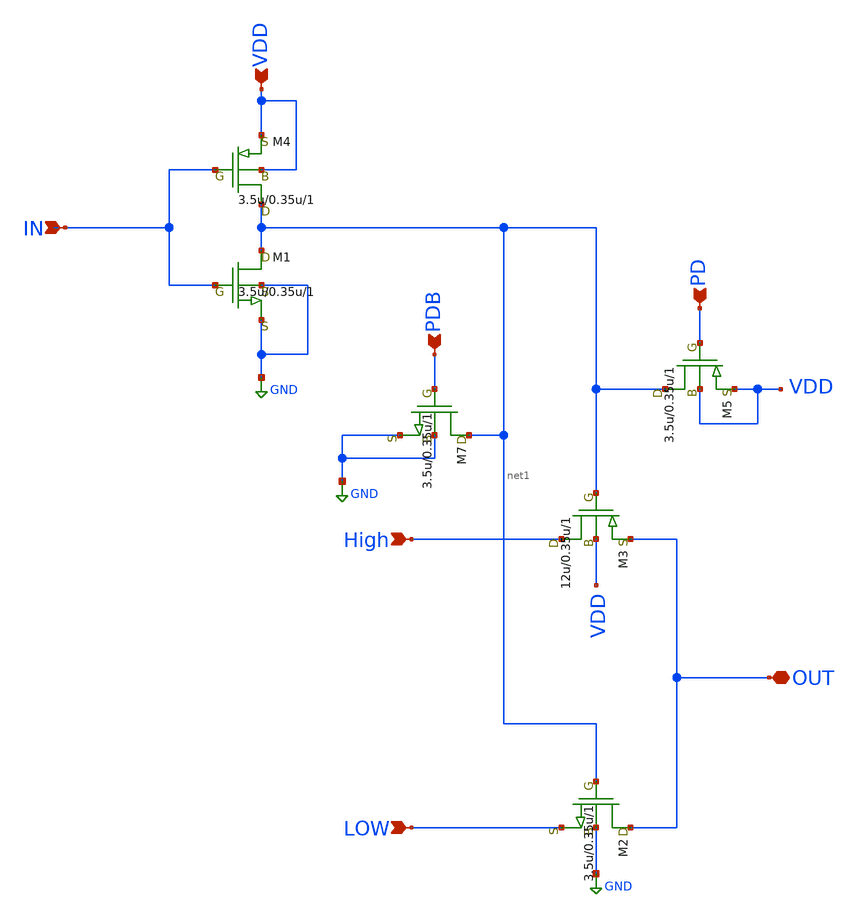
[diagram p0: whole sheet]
** sch_path: LR_Work5/RDAC_0128/SEL.sch
**.subckt SEL High LOW IN VDD OUT PD PDB
*.ipin High
*.ipin LOW
*.ipin IN
*.ipin VDD
*.iopin OUT
*.ipin PD
*.ipin PDB
M4 net1 IN VDD VDD p3.0 w=3.5u l=0.35u as=0 ps=0 ad=0 pd=0 m=1
M1 net1 IN GND GND n3.0 w=3.5u l=0.35u as=0 ps=0 ad=0 pd=0 m=1
M2 OUT net1 LOW GND n3.0 w=3.5u l=0.35u as=0 ps=0 ad=0 pd=0 m=1
M3 High net1 OUT VDD p3.0 w=12u l=0.35u as=0 ps=0 ad=0 pd=0 m=1
M5 net1 PD VDD VDD p3.0 w=3.5u l=0.35u as=0 ps=0 ad=0 pd=0 m=1
M7 net1 PDB GND GND n3.0 w=3.5u l=0.35u as=0 ps=0 ad=0 pd=0 m=1
**.ends
.GLOBAL GND
.end
